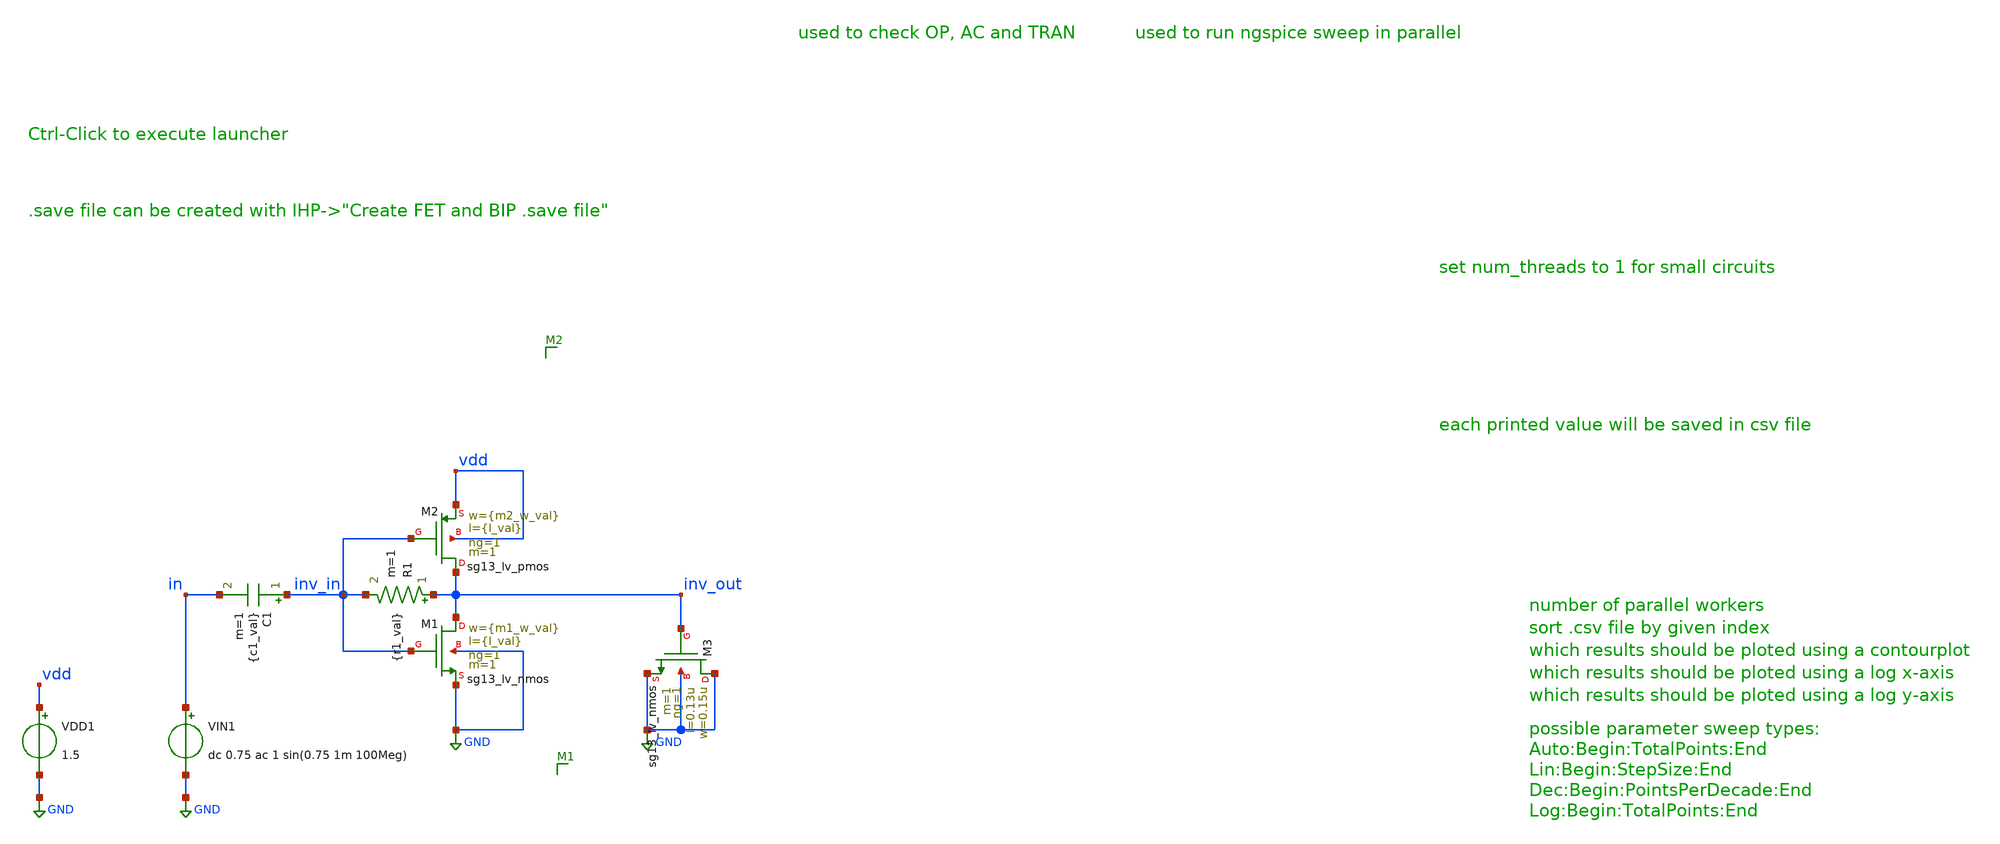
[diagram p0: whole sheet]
** sch_path: ihp-sg13g2/xschem_libs/sg13g2_tests_ase/inv_sweep_tb/schematic/inv_sweep_tb.sch
**.subckt inv_sweep_tb
VDD1 vdd GND 1.5
XM1 inv_out inv_in GND GND sg13_lv_nmos w={m1_w_val} l={l_val} ng=1 m=1 mm_ok=1
XM2 inv_out inv_in vdd vdd sg13_lv_pmos w={m2_w_val} l={l_val} ng=1 m=1 mm_ok=1
XM3 GND inv_out GND GND sg13_lv_nmos w=0.15u l=0.13u ng=1 m=1 mm_ok=1
VIN1 in GND dc 0.75 ac 1 sin(0.75 1m 100Meg)
R1 inv_out inv_in {r1_val} m=1
C1 inv_in in {c1_val} m=1
**.ends
.GLOBAL GND
.end
